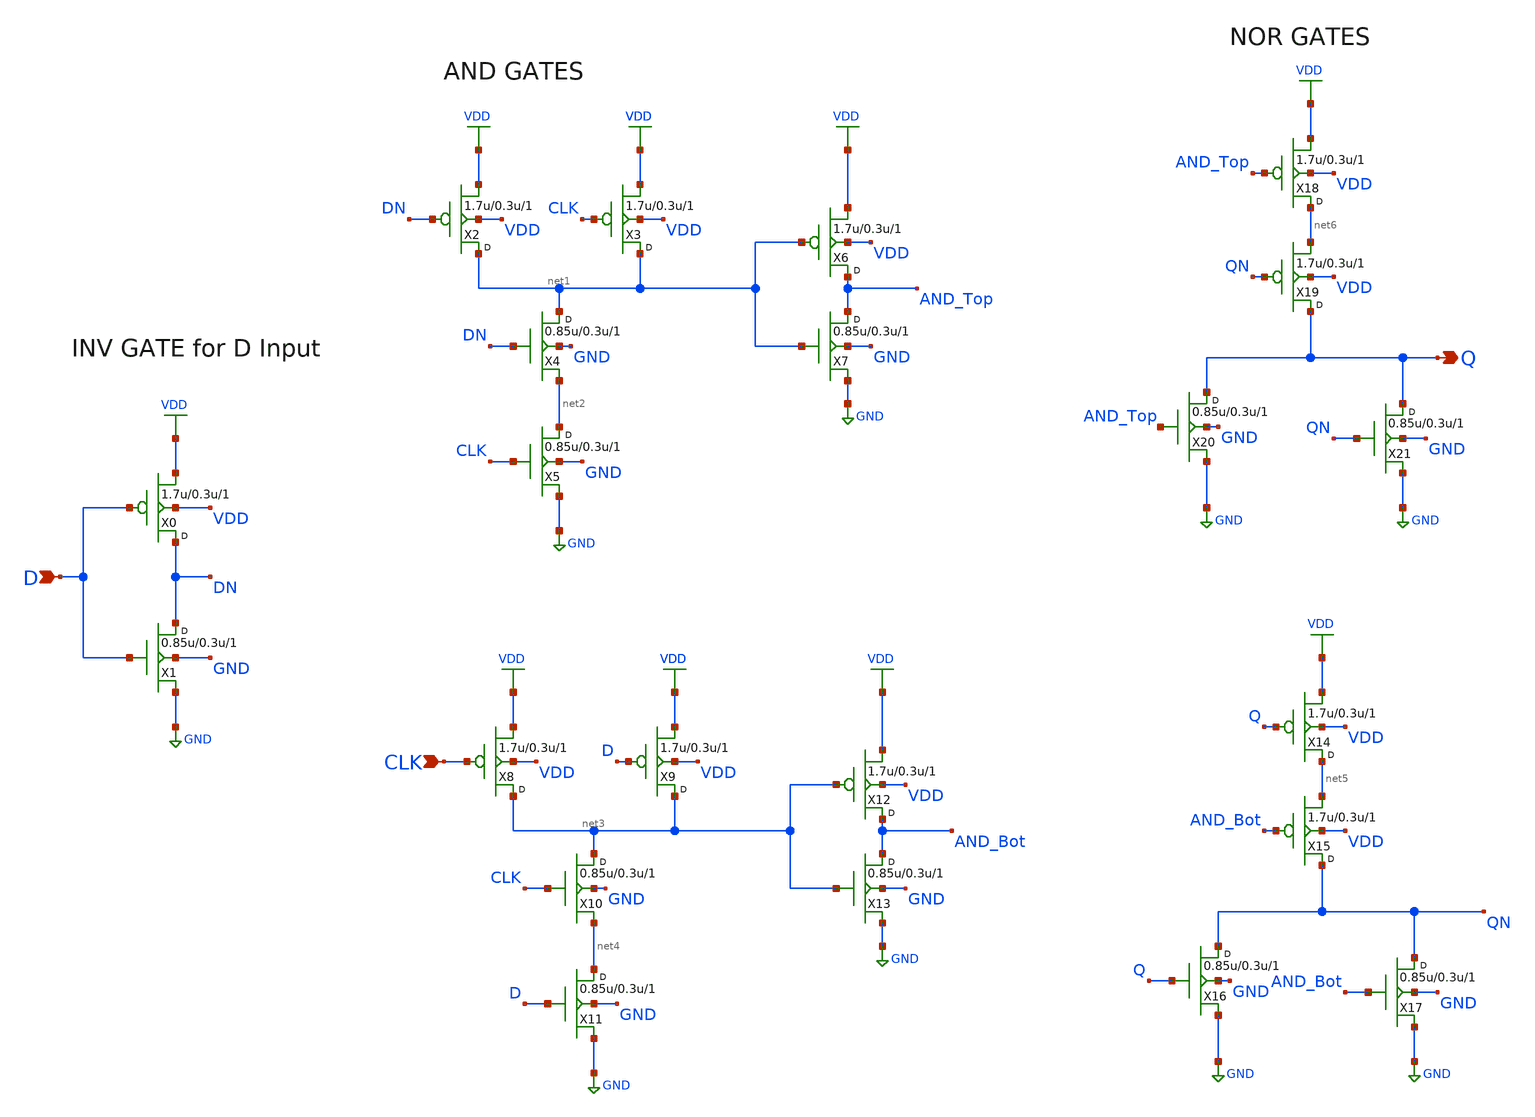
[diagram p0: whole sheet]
** sch_path: gf180mcu_osu_sc_gp9t3v3/cells/dlat/gf180mcu_osu_sc_gp9t3v3__dlat_1.sch
**.subckt gf180mcu_osu_sc_gp9t3v3__dlat_1 D CLK Q
*.ipin D
*.ipin CLK
*.opin Q
X0 DN D VDD VDD pfet_03p3 w=1.7u l=0.3u m=1
X1 DN D GND GND nfet_03p3 w=0.85u l=0.3u m=1
X2 net1 DN VDD VDD pfet_03p3 w=1.7u l=0.3u m=1
X3 net1 CLK VDD VDD pfet_03p3 w=1.7u l=0.3u m=1
X4 net1 DN net2 GND nfet_03p3 w=0.85u l=0.3u m=1
X5 net2 CLK GND GND nfet_03p3 w=0.85u l=0.3u m=1
X6 AND_Top net1 VDD VDD pfet_03p3 w=1.7u l=0.3u m=1
X7 AND_Top net1 GND GND nfet_03p3 w=0.85u l=0.3u m=1
X8 net3 CLK VDD VDD pfet_03p3 w=1.7u l=0.3u m=1
X9 net3 D VDD VDD pfet_03p3 w=1.7u l=0.3u m=1
X10 net3 CLK net4 GND nfet_03p3 w=0.85u l=0.3u m=1
X11 net4 D GND GND nfet_03p3 w=0.85u l=0.3u m=1
X12 AND_Bot net3 VDD VDD pfet_03p3 w=1.7u l=0.3u m=1
X13 AND_Bot net3 GND GND nfet_03p3 w=0.85u l=0.3u m=1
X14 net5 Q VDD VDD pfet_03p3 w=1.7u l=0.3u m=1
X15 QN AND_Bot net5 VDD pfet_03p3 w=1.7u l=0.3u m=1
X16 QN Q GND GND nfet_03p3 w=0.85u l=0.3u m=1
X17 QN AND_Bot GND GND nfet_03p3 w=0.85u l=0.3u m=1
X18 net6 AND_Top VDD VDD pfet_03p3 w=1.7u l=0.3u m=1
X19 Q QN net6 VDD pfet_03p3 w=1.7u l=0.3u m=1
X20 Q AND_Top GND GND nfet_03p3 w=0.85u l=0.3u m=1
X21 Q QN GND GND nfet_03p3 w=0.85u l=0.3u m=1
**.ends
.GLOBAL VDD
.GLOBAL GND
.end
